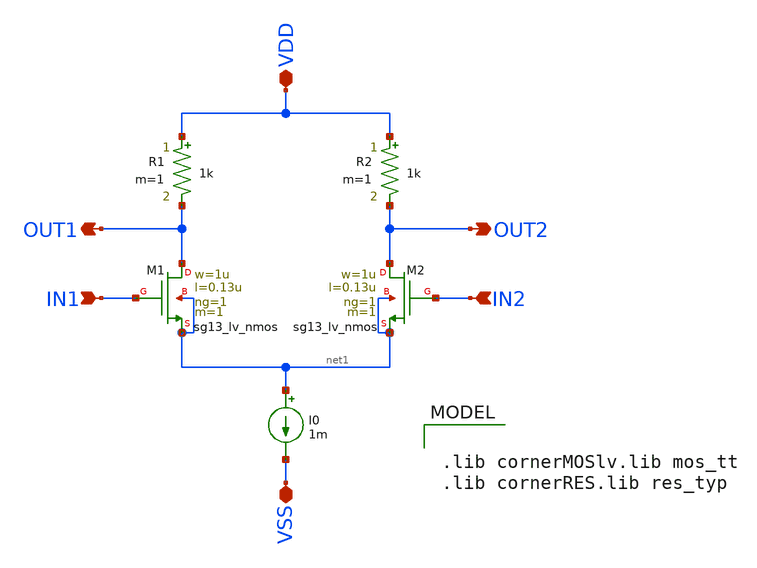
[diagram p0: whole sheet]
** sch_path: xschem/diff_pair.sch
**.subckt diff_pair VDD VSS IN1 IN2 OUT2 OUT1
*.iopin VDD
*.iopin VSS
*.ipin IN1
*.ipin IN2
*.opin OUT2
*.opin OUT1
XM1 OUT1 IN1 net1 net1 sg13_lv_nmos w=1u l=0.13u ng=1 m=1 mm_ok=1
XM2 OUT2 IN2 net1 net1 sg13_lv_nmos w=1u l=0.13u ng=1 m=1 mm_ok=1
I0 net1 VSS 1m
R1 VDD OUT1 1k m=1
R2 VDD OUT2 1k m=1
**** begin user architecture code


.lib cornerMOSlv.lib mos_tt
.lib cornerRES.lib res_typ


**** end user architecture code
**.ends
.end
